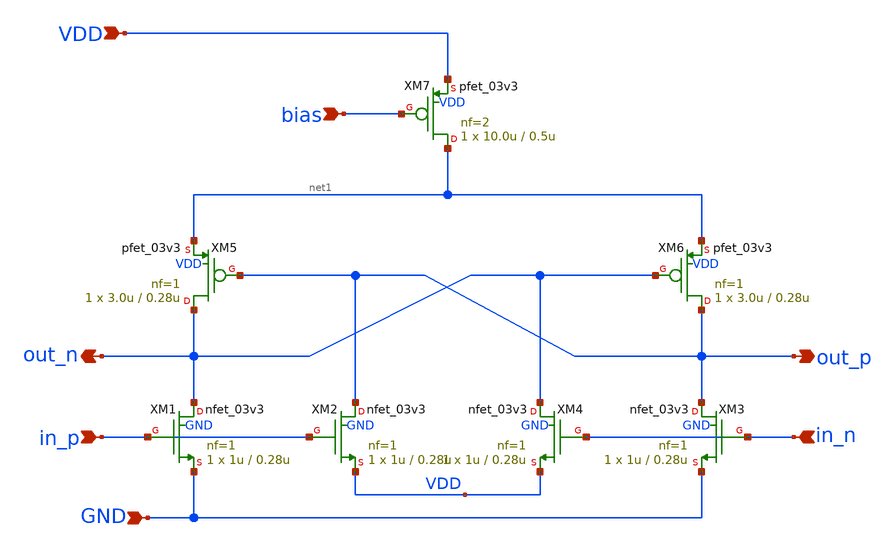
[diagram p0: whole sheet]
** sch_path: xschem/vco_dly_tt.sch
**.subckt vco_dly_tt out_p out_n in_p in_n bias VDD GND
*.opin out_p
*.opin out_n
*.ipin in_p
*.ipin in_n
*.ipin bias
*.ipin VDD
*.ipin GND
XM1 out_n in_p GND GND nfet_03v3 L=0.28u W=1u nf=1 ad='int((nf+1)/2) * W/nf * 0.18u' as='int((nf+2)/2) * W/nf * 0.18u'
+ pd='2*int((nf+1)/2) * (W/nf + 0.18u)' ps='2*int((nf+2)/2) * (W/nf + 0.18u)' nrd='0.18u / W' nrs='0.18u / W'
+ sa=0 sb=0 sd=0 m=1 par=1
XM2 out_p in_p VDD GND nfet_03v3 L=0.28u W=1u nf=1 ad='int((nf+1)/2) * W/nf * 0.18u' as='int((nf+2)/2) * W/nf * 0.18u'
+ pd='2*int((nf+1)/2) * (W/nf + 0.18u)' ps='2*int((nf+2)/2) * (W/nf + 0.18u)' nrd='0.18u / W' nrs='0.18u / W'
+ sa=0 sb=0 sd=0 m=1 par=1
XM3 out_p in_n GND GND nfet_03v3 L=0.28u W=1u nf=1 ad='int((nf+1)/2) * W/nf * 0.18u' as='int((nf+2)/2) * W/nf * 0.18u'
+ pd='2*int((nf+1)/2) * (W/nf + 0.18u)' ps='2*int((nf+2)/2) * (W/nf + 0.18u)' nrd='0.18u / W' nrs='0.18u / W'
+ sa=0 sb=0 sd=0 m=1 par=1
XM4 out_n in_n VDD GND nfet_03v3 L=0.28u W=1u nf=1 ad='int((nf+1)/2) * W/nf * 0.18u' as='int((nf+2)/2) * W/nf * 0.18u'
+ pd='2*int((nf+1)/2) * (W/nf + 0.18u)' ps='2*int((nf+2)/2) * (W/nf + 0.18u)' nrd='0.18u / W' nrs='0.18u / W'
+ sa=0 sb=0 sd=0 m=1 par=1
XM6 out_p out_n net1 VDD pfet_03v3 L=0.28u W=3.0u nf=1 ad='int((nf+1)/2) * W/nf * 0.18u' as='int((nf+2)/2) * W/nf * 0.18u'
+ pd='2*int((nf+1)/2) * (W/nf + 0.18u)' ps='2*int((nf+2)/2) * (W/nf + 0.18u)' nrd='0.18u / W' nrs='0.18u / W'
+ sa=0 sb=0 sd=0 m=1 par=1
XM5 out_n out_p net1 VDD pfet_03v3 L=0.28u W=3.0u nf=1 ad='int((nf+1)/2) * W/nf * 0.18u' as='int((nf+2)/2) * W/nf * 0.18u'
+ pd='2*int((nf+1)/2) * (W/nf + 0.18u)' ps='2*int((nf+2)/2) * (W/nf + 0.18u)' nrd='0.18u / W' nrs='0.18u / W'
+ sa=0 sb=0 sd=0 m=1 par=1
XM7 net1 bias VDD VDD pfet_03v3 L=0.5u W=10.0u nf=2 ad='int((nf+1)/2) * W/nf * 0.18u' as='int((nf+2)/2) * W/nf * 0.18u'
+ pd='2*int((nf+1)/2) * (W/nf + 0.18u)' ps='2*int((nf+2)/2) * (W/nf + 0.18u)' nrd='0.18u / W' nrs='0.18u / W'
+ sa=0 sb=0 sd=0 m=1 par=1
**.ends
.end
